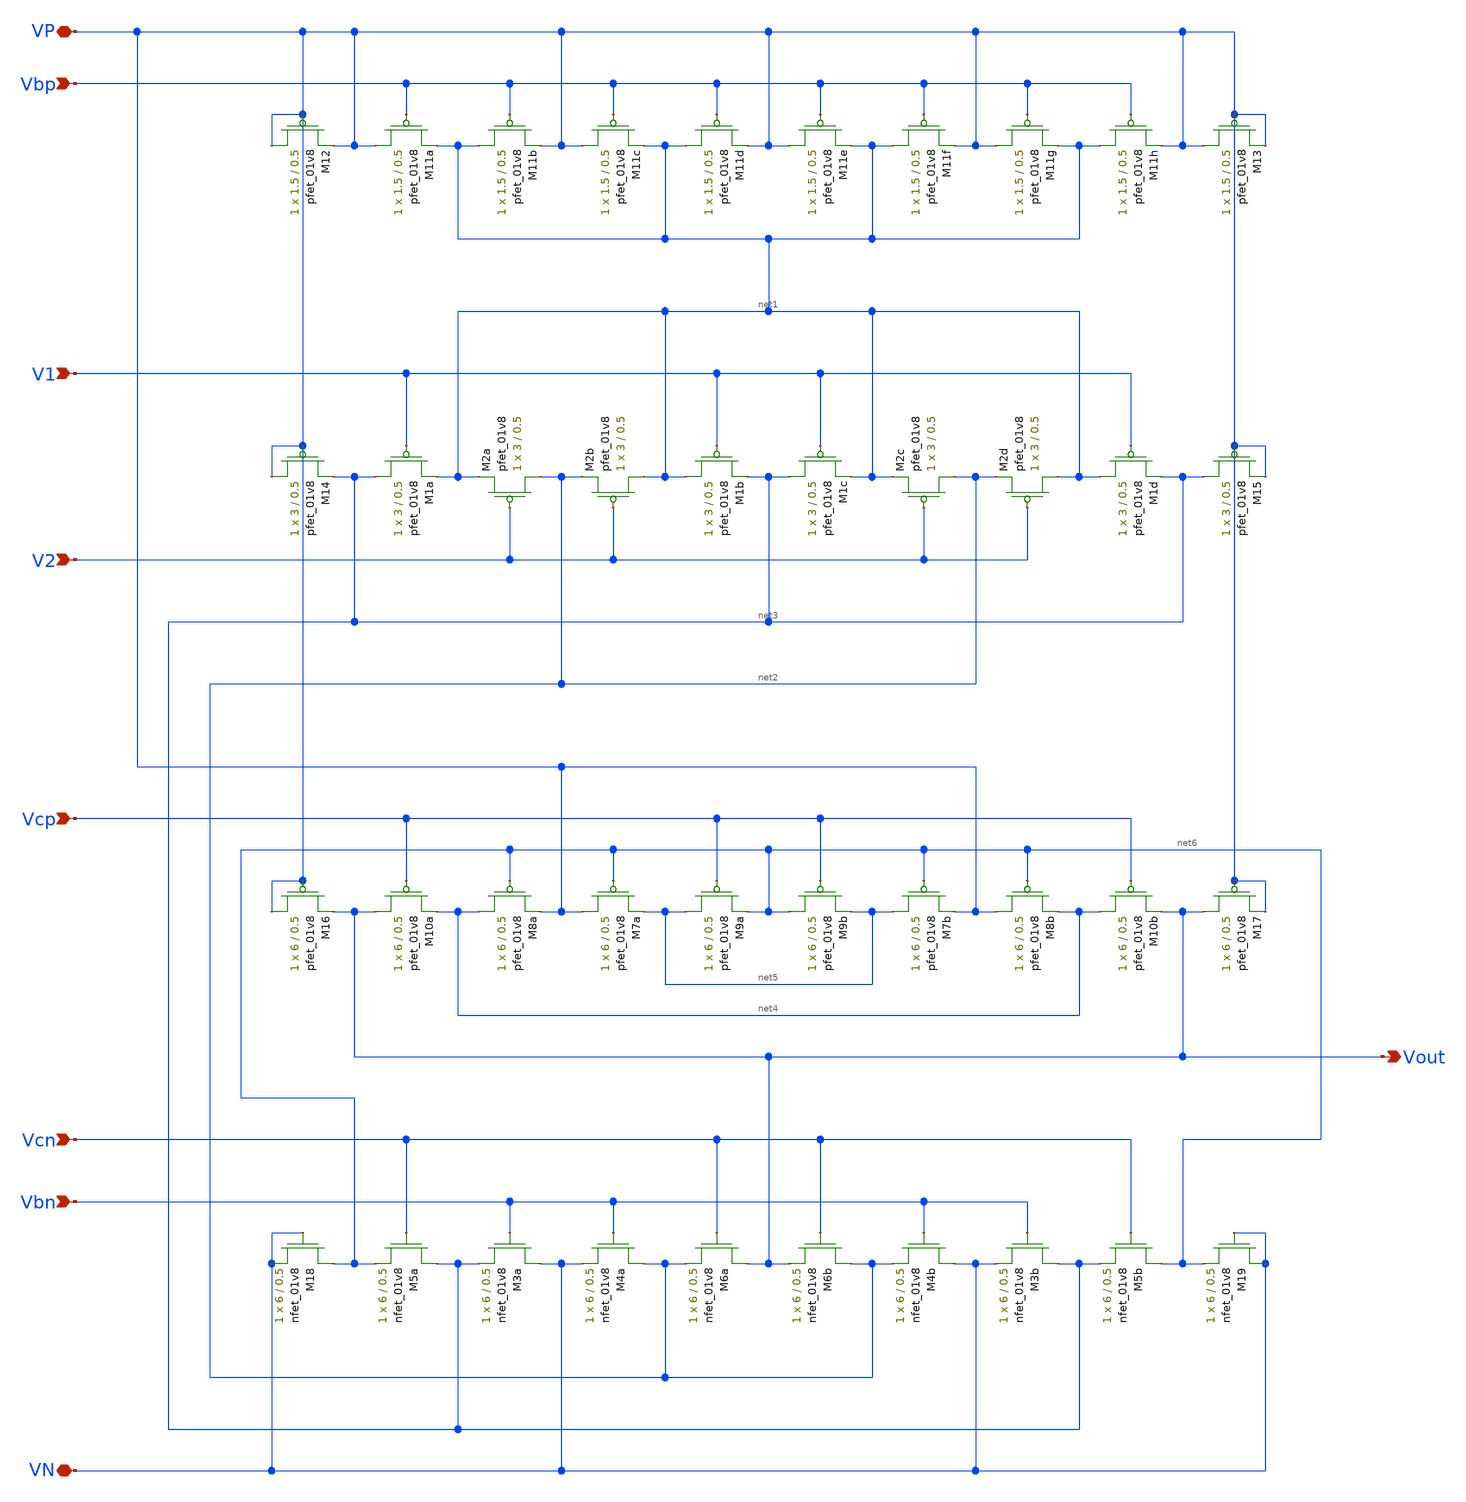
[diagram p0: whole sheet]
** sch_path: schematic/folded_cascode_differential_amplifier_LDS.sch
**.subckt folded_cascode_differential_amplifier_LDS Vbn Vcn Vcp V2 V1 Vbp VP VN Vout
*.ipin Vbn
*.ipin Vcn
*.ipin Vcp
*.ipin V2
*.ipin V1
*.ipin Vbp
*.iopin VP
*.iopin VN
*.opin Vout
XM5a net3 Vcn net6 GND sky130_fd_pr__nfet_01v8 L=0.5 W=6 nf=1 ad='int((nf+1)/2) * W/nf * 0.29' as='int((nf+2)/2) * W/nf * 0.29'
+ pd='2*int((nf+1)/2) * (W/nf + 0.29)' ps='2*int((nf+2)/2) * (W/nf + 0.29)' nrd='0.29 / W' nrs='0.29 / W'
+ sa=0 sb=0 sd=0 mult=1 m=1
XM1a net3 V1 net1 VDD sky130_fd_pr__pfet_01v8 L=0.5 W=3 nf=1 ad='int((nf+1)/2) * W/nf * 0.29' as='int((nf+2)/2) * W/nf * 0.29'
+ pd='2*int((nf+1)/2) * (W/nf + 0.29)' ps='2*int((nf+2)/2) * (W/nf + 0.29)' nrd='0.29 / W' nrs='0.29 / W'
+ sa=0 sb=0 sd=0 mult=1 m=1
XM2a net2 V2 net1 VDD sky130_fd_pr__pfet_01v8 L=0.5 W=3 nf=1 ad='int((nf+1)/2) * W/nf * 0.29' as='int((nf+2)/2) * W/nf * 0.29'
+ pd='2*int((nf+1)/2) * (W/nf + 0.29)' ps='2*int((nf+2)/2) * (W/nf + 0.29)' nrd='0.29 / W' nrs='0.29 / W'
+ sa=0 sb=0 sd=0 mult=1 m=1
XM2b net1 V2 net2 VDD sky130_fd_pr__pfet_01v8 L=0.5 W=3 nf=1 ad='int((nf+1)/2) * W/nf * 0.29' as='int((nf+2)/2) * W/nf * 0.29'
+ pd='2*int((nf+1)/2) * (W/nf + 0.29)' ps='2*int((nf+2)/2) * (W/nf + 0.29)' nrd='0.29 / W' nrs='0.29 / W'
+ sa=0 sb=0 sd=0 mult=1 m=1
XM1b net1 V1 net3 VDD sky130_fd_pr__pfet_01v8 L=0.5 W=3 nf=1 ad='int((nf+1)/2) * W/nf * 0.29' as='int((nf+2)/2) * W/nf * 0.29'
+ pd='2*int((nf+1)/2) * (W/nf + 0.29)' ps='2*int((nf+2)/2) * (W/nf + 0.29)' nrd='0.29 / W' nrs='0.29 / W'
+ sa=0 sb=0 sd=0 mult=1 m=1
XM1c net3 V1 net1 VDD sky130_fd_pr__pfet_01v8 L=0.5 W=3 nf=1 ad='int((nf+1)/2) * W/nf * 0.29' as='int((nf+2)/2) * W/nf * 0.29'
+ pd='2*int((nf+1)/2) * (W/nf + 0.29)' ps='2*int((nf+2)/2) * (W/nf + 0.29)' nrd='0.29 / W' nrs='0.29 / W'
+ sa=0 sb=0 sd=0 mult=1 m=1
XM2c net2 V2 net1 VDD sky130_fd_pr__pfet_01v8 L=0.5 W=3 nf=1 ad='int((nf+1)/2) * W/nf * 0.29' as='int((nf+2)/2) * W/nf * 0.29'
+ pd='2*int((nf+1)/2) * (W/nf + 0.29)' ps='2*int((nf+2)/2) * (W/nf + 0.29)' nrd='0.29 / W' nrs='0.29 / W'
+ sa=0 sb=0 sd=0 mult=1 m=1
XM2d net1 V2 net2 VDD sky130_fd_pr__pfet_01v8 L=0.5 W=3 nf=1 ad='int((nf+1)/2) * W/nf * 0.29' as='int((nf+2)/2) * W/nf * 0.29'
+ pd='2*int((nf+1)/2) * (W/nf + 0.29)' ps='2*int((nf+2)/2) * (W/nf + 0.29)' nrd='0.29 / W' nrs='0.29 / W'
+ sa=0 sb=0 sd=0 mult=1 m=1
XM1d net1 V1 net3 VDD sky130_fd_pr__pfet_01v8 L=0.5 W=3 nf=1 ad='int((nf+1)/2) * W/nf * 0.29' as='int((nf+2)/2) * W/nf * 0.29'
+ pd='2*int((nf+1)/2) * (W/nf + 0.29)' ps='2*int((nf+2)/2) * (W/nf + 0.29)' nrd='0.29 / W' nrs='0.29 / W'
+ sa=0 sb=0 sd=0 mult=1 m=1
XM11a VP Vbp net1 VDD sky130_fd_pr__pfet_01v8 L=0.5 W=1.5 nf=1 ad='int((nf+1)/2) * W/nf * 0.29' as='int((nf+2)/2) * W/nf * 0.29'
+ pd='2*int((nf+1)/2) * (W/nf + 0.29)' ps='2*int((nf+2)/2) * (W/nf + 0.29)' nrd='0.29 / W' nrs='0.29 / W'
+ sa=0 sb=0 sd=0 mult=1 m=1
XM11b net1 Vbp VP VDD sky130_fd_pr__pfet_01v8 L=0.5 W=1.5 nf=1 ad='int((nf+1)/2) * W/nf * 0.29' as='int((nf+2)/2) * W/nf * 0.29'
+ pd='2*int((nf+1)/2) * (W/nf + 0.29)' ps='2*int((nf+2)/2) * (W/nf + 0.29)' nrd='0.29 / W' nrs='0.29 / W'
+ sa=0 sb=0 sd=0 mult=1 m=1
XM11c VP Vbp net1 VDD sky130_fd_pr__pfet_01v8 L=0.5 W=1.5 nf=1 ad='int((nf+1)/2) * W/nf * 0.29' as='int((nf+2)/2) * W/nf * 0.29'
+ pd='2*int((nf+1)/2) * (W/nf + 0.29)' ps='2*int((nf+2)/2) * (W/nf + 0.29)' nrd='0.29 / W' nrs='0.29 / W'
+ sa=0 sb=0 sd=0 mult=1 m=1
XM11d net1 Vbp VP VDD sky130_fd_pr__pfet_01v8 L=0.5 W=1.5 nf=1 ad='int((nf+1)/2) * W/nf * 0.29' as='int((nf+2)/2) * W/nf * 0.29'
+ pd='2*int((nf+1)/2) * (W/nf + 0.29)' ps='2*int((nf+2)/2) * (W/nf + 0.29)' nrd='0.29 / W' nrs='0.29 / W'
+ sa=0 sb=0 sd=0 mult=1 m=1
XM11e VP Vbp net1 VDD sky130_fd_pr__pfet_01v8 L=0.5 W=1.5 nf=1 ad='int((nf+1)/2) * W/nf * 0.29' as='int((nf+2)/2) * W/nf * 0.29'
+ pd='2*int((nf+1)/2) * (W/nf + 0.29)' ps='2*int((nf+2)/2) * (W/nf + 0.29)' nrd='0.29 / W' nrs='0.29 / W'
+ sa=0 sb=0 sd=0 mult=1 m=1
XM11f net1 Vbp VP VDD sky130_fd_pr__pfet_01v8 L=0.5 W=1.5 nf=1 ad='int((nf+1)/2) * W/nf * 0.29' as='int((nf+2)/2) * W/nf * 0.29'
+ pd='2*int((nf+1)/2) * (W/nf + 0.29)' ps='2*int((nf+2)/2) * (W/nf + 0.29)' nrd='0.29 / W' nrs='0.29 / W'
+ sa=0 sb=0 sd=0 mult=1 m=1
XM11g VP Vbp net1 VDD sky130_fd_pr__pfet_01v8 L=0.5 W=1.5 nf=1 ad='int((nf+1)/2) * W/nf * 0.29' as='int((nf+2)/2) * W/nf * 0.29'
+ pd='2*int((nf+1)/2) * (W/nf + 0.29)' ps='2*int((nf+2)/2) * (W/nf + 0.29)' nrd='0.29 / W' nrs='0.29 / W'
+ sa=0 sb=0 sd=0 mult=1 m=1
XM11h net1 Vbp VP VDD sky130_fd_pr__pfet_01v8 L=0.5 W=1.5 nf=1 ad='int((nf+1)/2) * W/nf * 0.29' as='int((nf+2)/2) * W/nf * 0.29'
+ pd='2*int((nf+1)/2) * (W/nf + 0.29)' ps='2*int((nf+2)/2) * (W/nf + 0.29)' nrd='0.29 / W' nrs='0.29 / W'
+ sa=0 sb=0 sd=0 mult=1 m=1
XM3a VN Vbn net3 GND sky130_fd_pr__nfet_01v8 L=0.5 W=6 nf=1 ad='int((nf+1)/2) * W/nf * 0.29' as='int((nf+2)/2) * W/nf * 0.29'
+ pd='2*int((nf+1)/2) * (W/nf + 0.29)' ps='2*int((nf+2)/2) * (W/nf + 0.29)' nrd='0.29 / W' nrs='0.29 / W'
+ sa=0 sb=0 sd=0 mult=1 m=1
XM4a net2 Vbn VN GND sky130_fd_pr__nfet_01v8 L=0.5 W=6 nf=1 ad='int((nf+1)/2) * W/nf * 0.29' as='int((nf+2)/2) * W/nf * 0.29'
+ pd='2*int((nf+1)/2) * (W/nf + 0.29)' ps='2*int((nf+2)/2) * (W/nf + 0.29)' nrd='0.29 / W' nrs='0.29 / W'
+ sa=0 sb=0 sd=0 mult=1 m=1
XM6a Vout Vcn net2 GND sky130_fd_pr__nfet_01v8 L=0.5 W=6 nf=1 ad='int((nf+1)/2) * W/nf * 0.29' as='int((nf+2)/2) * W/nf * 0.29'
+ pd='2*int((nf+1)/2) * (W/nf + 0.29)' ps='2*int((nf+2)/2) * (W/nf + 0.29)' nrd='0.29 / W' nrs='0.29 / W'
+ sa=0 sb=0 sd=0 mult=1 m=1
XM6b net2 Vcn Vout GND sky130_fd_pr__nfet_01v8 L=0.5 W=6 nf=1 ad='int((nf+1)/2) * W/nf * 0.29' as='int((nf+2)/2) * W/nf * 0.29'
+ pd='2*int((nf+1)/2) * (W/nf + 0.29)' ps='2*int((nf+2)/2) * (W/nf + 0.29)' nrd='0.29 / W' nrs='0.29 / W'
+ sa=0 sb=0 sd=0 mult=1 m=1
XM4b VN Vbn net2 GND sky130_fd_pr__nfet_01v8 L=0.5 W=6 nf=1 ad='int((nf+1)/2) * W/nf * 0.29' as='int((nf+2)/2) * W/nf * 0.29'
+ pd='2*int((nf+1)/2) * (W/nf + 0.29)' ps='2*int((nf+2)/2) * (W/nf + 0.29)' nrd='0.29 / W' nrs='0.29 / W'
+ sa=0 sb=0 sd=0 mult=1 m=1
XM3b net3 Vbn VN GND sky130_fd_pr__nfet_01v8 L=0.5 W=6 nf=1 ad='int((nf+1)/2) * W/nf * 0.29' as='int((nf+2)/2) * W/nf * 0.29'
+ pd='2*int((nf+1)/2) * (W/nf + 0.29)' ps='2*int((nf+2)/2) * (W/nf + 0.29)' nrd='0.29 / W' nrs='0.29 / W'
+ sa=0 sb=0 sd=0 mult=1 m=1
XM5b net6 Vcn net3 GND sky130_fd_pr__nfet_01v8 L=0.5 W=6 nf=1 ad='int((nf+1)/2) * W/nf * 0.29' as='int((nf+2)/2) * W/nf * 0.29'
+ pd='2*int((nf+1)/2) * (W/nf + 0.29)' ps='2*int((nf+2)/2) * (W/nf + 0.29)' nrd='0.29 / W' nrs='0.29 / W'
+ sa=0 sb=0 sd=0 mult=1 m=1
XM10a Vout Vcp net4 VDD sky130_fd_pr__pfet_01v8 L=0.5 W=6 nf=1 ad='int((nf+1)/2) * W/nf * 0.29' as='int((nf+2)/2) * W/nf * 0.29'
+ pd='2*int((nf+1)/2) * (W/nf + 0.29)' ps='2*int((nf+2)/2) * (W/nf + 0.29)' nrd='0.29 / W' nrs='0.29 / W'
+ sa=0 sb=0 sd=0 mult=1 m=1
XM8a net4 net6 VP VDD sky130_fd_pr__pfet_01v8 L=0.5 W=6 nf=1 ad='int((nf+1)/2) * W/nf * 0.29' as='int((nf+2)/2) * W/nf * 0.29'
+ pd='2*int((nf+1)/2) * (W/nf + 0.29)' ps='2*int((nf+2)/2) * (W/nf + 0.29)' nrd='0.29 / W' nrs='0.29 / W'
+ sa=0 sb=0 sd=0 mult=1 m=1
XM7a VP net6 net5 VDD sky130_fd_pr__pfet_01v8 L=0.5 W=6 nf=1 ad='int((nf+1)/2) * W/nf * 0.29' as='int((nf+2)/2) * W/nf * 0.29'
+ pd='2*int((nf+1)/2) * (W/nf + 0.29)' ps='2*int((nf+2)/2) * (W/nf + 0.29)' nrd='0.29 / W' nrs='0.29 / W'
+ sa=0 sb=0 sd=0 mult=1 m=1
XM9a net5 Vcp net6 VDD sky130_fd_pr__pfet_01v8 L=0.5 W=6 nf=1 ad='int((nf+1)/2) * W/nf * 0.29' as='int((nf+2)/2) * W/nf * 0.29'
+ pd='2*int((nf+1)/2) * (W/nf + 0.29)' ps='2*int((nf+2)/2) * (W/nf + 0.29)' nrd='0.29 / W' nrs='0.29 / W'
+ sa=0 sb=0 sd=0 mult=1 m=1
XM9b net6 Vcp net5 VDD sky130_fd_pr__pfet_01v8 L=0.5 W=6 nf=1 ad='int((nf+1)/2) * W/nf * 0.29' as='int((nf+2)/2) * W/nf * 0.29'
+ pd='2*int((nf+1)/2) * (W/nf + 0.29)' ps='2*int((nf+2)/2) * (W/nf + 0.29)' nrd='0.29 / W' nrs='0.29 / W'
+ sa=0 sb=0 sd=0 mult=1 m=1
XM7b net5 net6 VP VDD sky130_fd_pr__pfet_01v8 L=0.5 W=6 nf=1 ad='int((nf+1)/2) * W/nf * 0.29' as='int((nf+2)/2) * W/nf * 0.29'
+ pd='2*int((nf+1)/2) * (W/nf + 0.29)' ps='2*int((nf+2)/2) * (W/nf + 0.29)' nrd='0.29 / W' nrs='0.29 / W'
+ sa=0 sb=0 sd=0 mult=1 m=1
XM8b VP net6 net4 VDD sky130_fd_pr__pfet_01v8 L=0.5 W=6 nf=1 ad='int((nf+1)/2) * W/nf * 0.29' as='int((nf+2)/2) * W/nf * 0.29'
+ pd='2*int((nf+1)/2) * (W/nf + 0.29)' ps='2*int((nf+2)/2) * (W/nf + 0.29)' nrd='0.29 / W' nrs='0.29 / W'
+ sa=0 sb=0 sd=0 mult=1 m=1
XM10b net4 Vcp Vout VDD sky130_fd_pr__pfet_01v8 L=0.5 W=6 nf=1 ad='int((nf+1)/2) * W/nf * 0.29' as='int((nf+2)/2) * W/nf * 0.29'
+ pd='2*int((nf+1)/2) * (W/nf + 0.29)' ps='2*int((nf+2)/2) * (W/nf + 0.29)' nrd='0.29 / W' nrs='0.29 / W'
+ sa=0 sb=0 sd=0 mult=1 m=1
XM15 net3 VP VP VDD sky130_fd_pr__pfet_01v8 L=0.5 W=3 nf=1 ad='int((nf+1)/2) * W/nf * 0.29' as='int((nf+2)/2) * W/nf * 0.29'
+ pd='2*int((nf+1)/2) * (W/nf + 0.29)' ps='2*int((nf+2)/2) * (W/nf + 0.29)' nrd='0.29 / W' nrs='0.29 / W'
+ sa=0 sb=0 sd=0 mult=1 m=1
XM14 VP VP net3 VDD sky130_fd_pr__pfet_01v8 L=0.5 W=3 nf=1 ad='int((nf+1)/2) * W/nf * 0.29' as='int((nf+2)/2) * W/nf * 0.29'
+ pd='2*int((nf+1)/2) * (W/nf + 0.29)' ps='2*int((nf+2)/2) * (W/nf + 0.29)' nrd='0.29 / W' nrs='0.29 / W'
+ sa=0 sb=0 sd=0 mult=1 m=1
XM13 VP VP VP VDD sky130_fd_pr__pfet_01v8 L=0.5 W=1.5 nf=1 ad='int((nf+1)/2) * W/nf * 0.29' as='int((nf+2)/2) * W/nf * 0.29'
+ pd='2*int((nf+1)/2) * (W/nf + 0.29)' ps='2*int((nf+2)/2) * (W/nf + 0.29)' nrd='0.29 / W' nrs='0.29 / W'
+ sa=0 sb=0 sd=0 mult=1 m=1
XM12 VP VP VP VDD sky130_fd_pr__pfet_01v8 L=0.5 W=1.5 nf=1 ad='int((nf+1)/2) * W/nf * 0.29' as='int((nf+2)/2) * W/nf * 0.29'
+ pd='2*int((nf+1)/2) * (W/nf + 0.29)' ps='2*int((nf+2)/2) * (W/nf + 0.29)' nrd='0.29 / W' nrs='0.29 / W'
+ sa=0 sb=0 sd=0 mult=1 m=1
XM16 VP VP Vout VDD sky130_fd_pr__pfet_01v8 L=0.5 W=6 nf=1 ad='int((nf+1)/2) * W/nf * 0.29' as='int((nf+2)/2) * W/nf * 0.29'
+ pd='2*int((nf+1)/2) * (W/nf + 0.29)' ps='2*int((nf+2)/2) * (W/nf + 0.29)' nrd='0.29 / W' nrs='0.29 / W'
+ sa=0 sb=0 sd=0 mult=1 m=1
XM17 Vout VP VP VDD sky130_fd_pr__pfet_01v8 L=0.5 W=6 nf=1 ad='int((nf+1)/2) * W/nf * 0.29' as='int((nf+2)/2) * W/nf * 0.29'
+ pd='2*int((nf+1)/2) * (W/nf + 0.29)' ps='2*int((nf+2)/2) * (W/nf + 0.29)' nrd='0.29 / W' nrs='0.29 / W'
+ sa=0 sb=0 sd=0 mult=1 m=1
XM19 VN VN net6 GND sky130_fd_pr__nfet_01v8 L=0.5 W=6 nf=1 ad='int((nf+1)/2) * W/nf * 0.29' as='int((nf+2)/2) * W/nf * 0.29'
+ pd='2*int((nf+1)/2) * (W/nf + 0.29)' ps='2*int((nf+2)/2) * (W/nf + 0.29)' nrd='0.29 / W' nrs='0.29 / W'
+ sa=0 sb=0 sd=0 mult=1 m=1
XM18 net6 VN VN GND sky130_fd_pr__nfet_01v8 L=0.5 W=6 nf=1 ad='int((nf+1)/2) * W/nf * 0.29' as='int((nf+2)/2) * W/nf * 0.29'
+ pd='2*int((nf+1)/2) * (W/nf + 0.29)' ps='2*int((nf+2)/2) * (W/nf + 0.29)' nrd='0.29 / W' nrs='0.29 / W'
+ sa=0 sb=0 sd=0 mult=1 m=1
**.ends
.end
